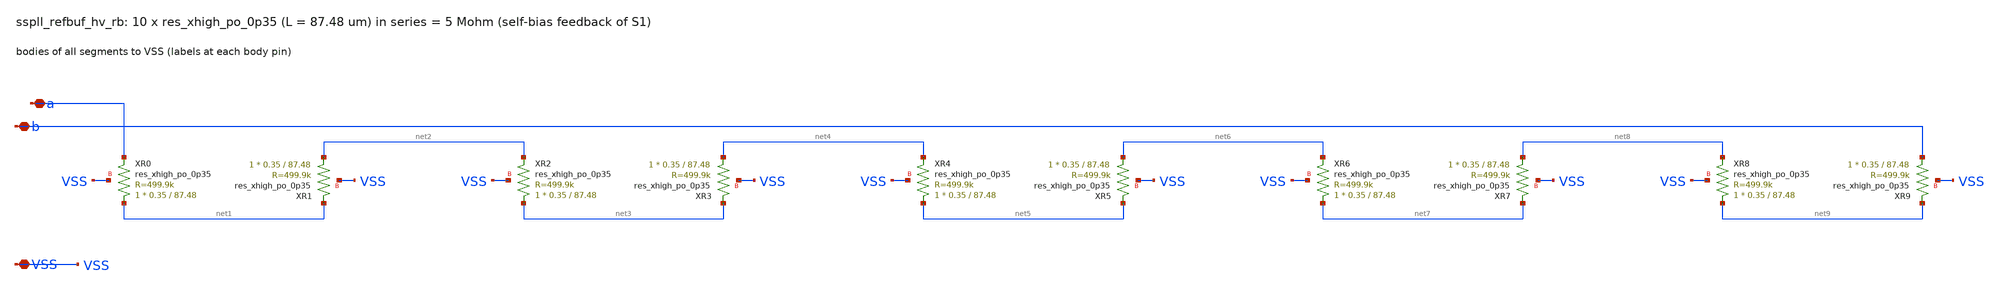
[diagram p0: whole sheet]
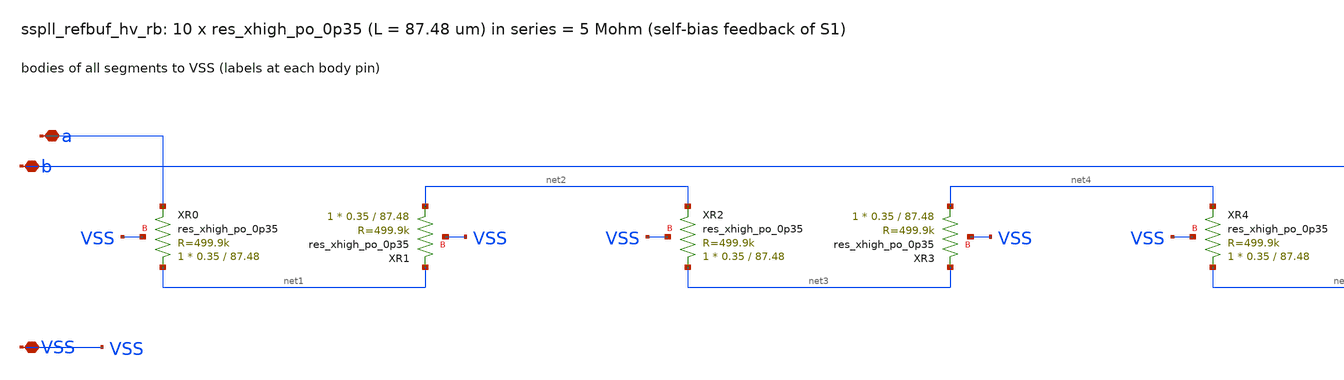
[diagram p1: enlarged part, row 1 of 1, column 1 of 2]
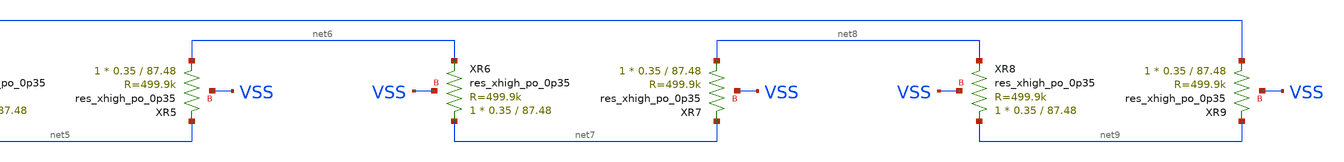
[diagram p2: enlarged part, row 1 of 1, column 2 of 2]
** sch_path: xschem/refbuf_hv/sspll_refbuf_hv_rb.sch
**.subckt sspll_refbuf_hv_rb a b VSS
*.iopin a
*.iopin b
*.iopin VSS
XXR0 net1 a VSS sky130_fd_pr__res_xhigh_po_0p35 L=87.48 mult=1 m=1
XXR1 net2 net1 VSS sky130_fd_pr__res_xhigh_po_0p35 L=87.48 mult=1 m=1
XXR2 net3 net2 VSS sky130_fd_pr__res_xhigh_po_0p35 L=87.48 mult=1 m=1
XXR3 net4 net3 VSS sky130_fd_pr__res_xhigh_po_0p35 L=87.48 mult=1 m=1
XXR4 net5 net4 VSS sky130_fd_pr__res_xhigh_po_0p35 L=87.48 mult=1 m=1
XXR5 net6 net5 VSS sky130_fd_pr__res_xhigh_po_0p35 L=87.48 mult=1 m=1
XXR6 net7 net6 VSS sky130_fd_pr__res_xhigh_po_0p35 L=87.48 mult=1 m=1
XXR7 net8 net7 VSS sky130_fd_pr__res_xhigh_po_0p35 L=87.48 mult=1 m=1
XXR8 net9 net8 VSS sky130_fd_pr__res_xhigh_po_0p35 L=87.48 mult=1 m=1
XXR9 b net9 VSS sky130_fd_pr__res_xhigh_po_0p35 L=87.48 mult=1 m=1
**.ends
.end
